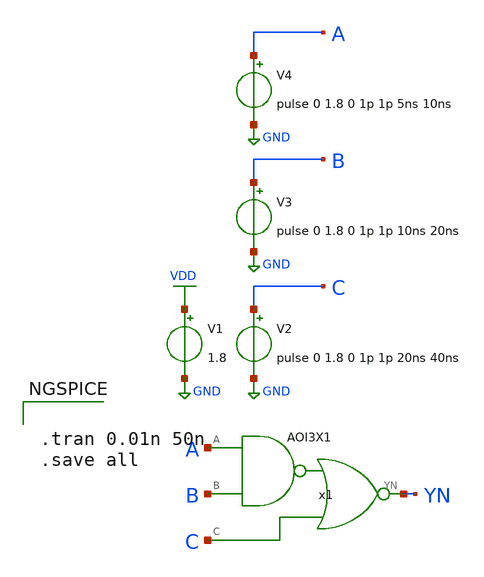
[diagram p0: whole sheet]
** sch_path: current/xschem/test_AOI3X1.sch
**.subckt test_AOI3X1
V2 C GND pulse 0 1.8 0 1p 1p 20ns 40ns
V1 VDD GND 1.8
V3 B GND pulse 0 1.8 0 1p 1p 10ns 20ns
V4 A GND pulse 0 1.8 0 1p 1p 5ns 10ns
x1 YN A B C VDD GND AOI3X1
**** begin user architecture code

.lib $::SKYWATER_MODELS/sky130.lib.spice tt


**** end user architecture code
**.ends
.GLOBAL VDD
.GLOBAL GND
**** begin user architecture code


.tran 0.01n 50n
.save all


**** end user architecture code
.end
